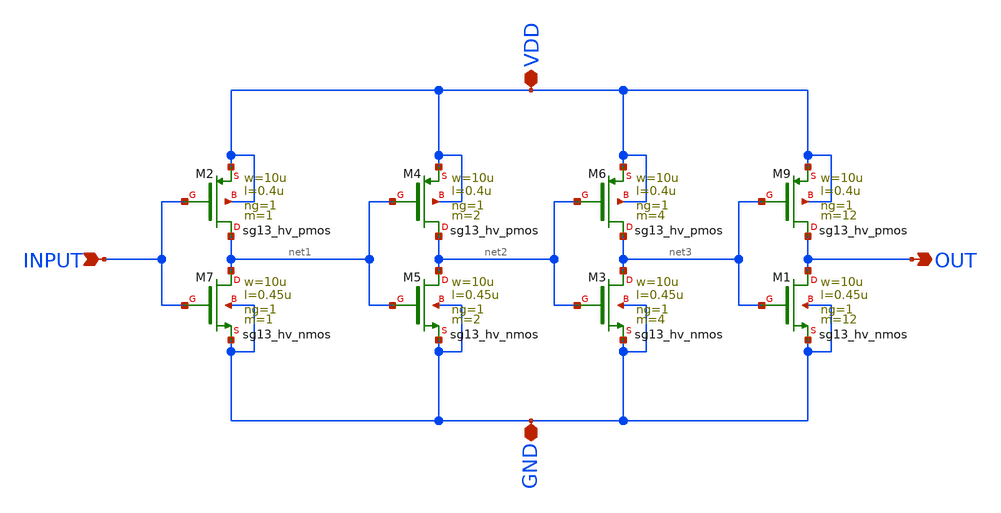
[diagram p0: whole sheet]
** sch_path: PLL0663-main/schematic/xschem/buf/buf.sch
**.subckt buf INPUT VDD GND OUT
*.ipin INPUT
*.iopin VDD
*.iopin GND
*.opin OUT
XM9 OUT net3 VDD VDD sg13_hv_pmos w=10u l=0.4u ng=1 m=12 mm_ok=1
XM6 net3 net2 VDD VDD sg13_hv_pmos w=10u l=0.4u ng=1 m=4 mm_ok=1
XM4 net2 net1 VDD VDD sg13_hv_pmos w=10u l=0.4u ng=1 m=2 mm_ok=1
XM2 net1 INPUT VDD VDD sg13_hv_pmos w=10u l=0.4u ng=1 m=1 mm_ok=1
XM1 OUT net3 GND GND sg13_hv_nmos w=10u l=0.45u ng=1 m=12 mm_ok=1
XM3 net3 net2 GND GND sg13_hv_nmos w=10u l=0.45u ng=1 m=4 mm_ok=1
XM5 net2 net1 GND GND sg13_hv_nmos w=10u l=0.45u ng=1 m=2 mm_ok=1
XM7 net1 INPUT GND GND sg13_hv_nmos w=10u l=0.45u ng=1 m=1 mm_ok=1
**.ends
.end
